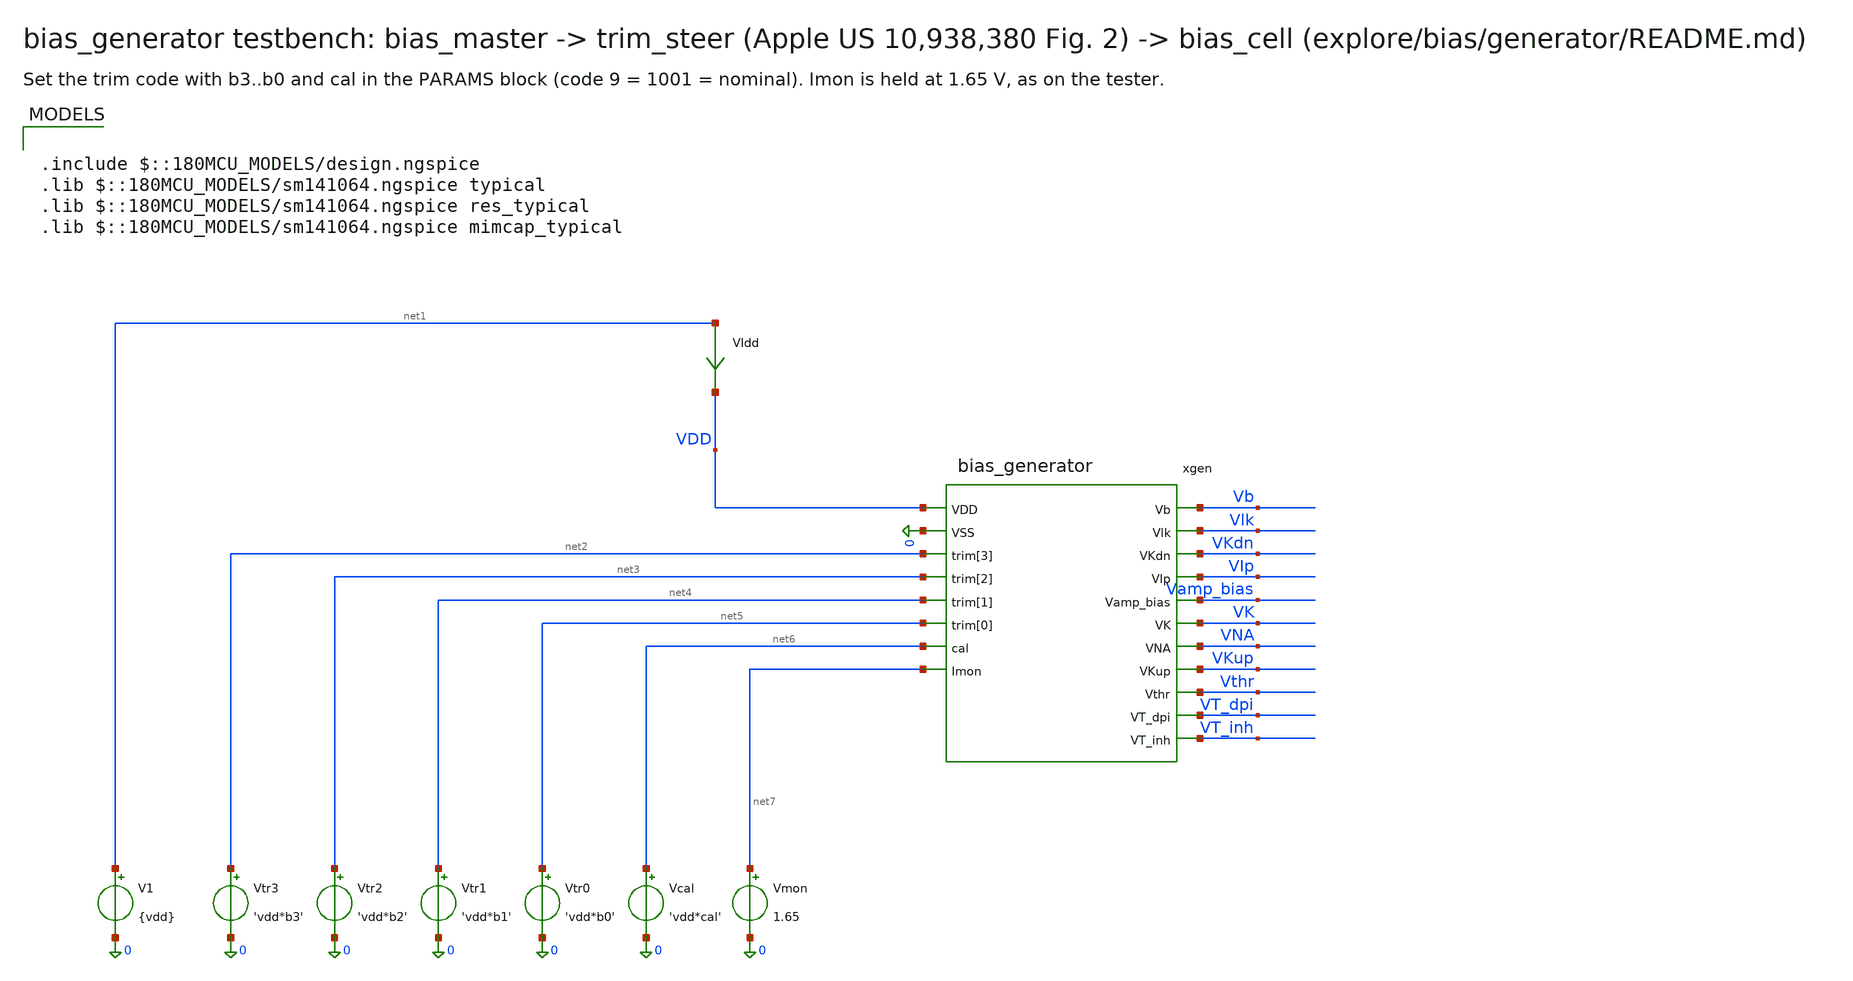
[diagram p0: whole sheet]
** sch_path: explore/bias/generator/bias_generator_tb.sch
**.subckt bias_generator_tb
xgen VDD 0 net2 net3 net4 net5 net6 net7 Vb Vlk VKdn VIp Vamp_bias VK VNA VKup Vthr VT_dpi VT_inh
+ bias_generator
V1 net1 0 {vdd}
VIdd net1 VDD 0
.save i(vidd)
Vtr3 net2 0 'vdd*b3'
Vtr2 net3 0 'vdd*b2'
Vtr1 net4 0 'vdd*b1'
Vtr0 net5 0 'vdd*b0'
Vcal net6 0 'vdd*cal'
Vmon net7 0 1.65
.save i(vmon)
**** begin user architecture code

.include $::180MCU_MODELS/design.ngspice
.lib $::180MCU_MODELS/sm141064.ngspice typical
.lib $::180MCU_MODELS/sm141064.ngspice res_typical
.lib $::180MCU_MODELS/sm141064.ngspice mimcap_typical



* trim code 9 = 1001 (nominal); ss chips trim to about 14, ff to about 4
* cal = 1 while trimming (aux path on: glitch-free code changes), 0 afterwards
.param vdd=3.3 b3=1 b2=0 b1=0 b0=1 cal=0
.temp 27




.control
save all
op
let imon_nA = -i(Vmon)*1e9
let supply_uA = i(VIdd)*1e6
print imon_nA supply_uA
print v(Vb) v(Vlk) v(VKdn) v(VIp) v(Vamp_bias) v(VK) v(VNA) v(VKup) v(Vthr) v(VT_dpi) v(VT_inh)
dc V1 2.97 3.63 0.03
plot v(Vb) v(Vlk) v(VKdn) v(VIp)
.endc


**** end user architecture code
**.ends

* expanding   symbol:  explore/bias/generator/bias_generator.sym # of pins=19
** sym_path: analog/bias/generator/bias_generator.sym
** sch_path: analog/bias/generator/bias_generator.sch
.subckt bias_generator VDD VSS trim[3] trim[2] trim[1] trim[0] cal Imon Vb Vlk VKdn VIp Vamp_bias VK
+ VNA VKup Vthr VT_dpi VT_inh
*.iopin VDD
*.iopin VSS
*.ipin trim[3]
*.ipin trim[2]
*.ipin trim[1]
*.ipin trim[0]
*.ipin cal
*.iopin Imon
*.opin Vb
*.opin Vlk
*.opin VKdn
*.opin VIp
*.opin Vamp_bias
*.opin VK
*.opin VNA
*.opin VKup
*.opin Vthr
*.opin VT_dpi
*.opin VT_inh
xmaster VDD VSS Iref bias_master
xtrim VDD VSS Iref Ibias trim[3] trim[2] trim[1] trim[0] cal trim_steer
xcell VDD VSS Ibias Vb Vlk VKdn VIp Vamp_bias VK VNA VKup Vthr VT_dpi VT_inh bias_cell
XMMON Imon Ibias VSS VSS nfet_03v3 L=8.0u W=10.0u nf=1 ad='int((nf+1)/2) * W/nf * 0.18u' as='int((nf+2)/2) * W/nf * 0.18u'
+ pd='2*int((nf+1)/2) * (W/nf + 0.18u)' ps='2*int((nf+2)/2) * (W/nf + 0.18u)' nrd='0.18u / W' nrs='0.18u / W'
+ sa=0 sb=0 sd=0 m=1
.ends


* expanding   symbol:  analog/bias/generator/bias_master.sym # of pins=3
** sym_path: analog/bias/generator/bias_master.sym
** sch_path: analog/bias/generator/bias_master.sch
.subckt bias_master VDD VSS Iref
*.iopin VDD
*.iopin VSS
*.iopin Iref
XM3 Vgp Vgp VDD VDD pfet_03v3 L=6.0u W=1.0u nf=1 ad='int((nf+1)/2) * W/nf * 0.18u' as='int((nf+2)/2) * W/nf * 0.18u'
+ pd='2*int((nf+1)/2) * (W/nf + 0.18u)' ps='2*int((nf+2)/2) * (W/nf + 0.18u)' nrd='0.18u / W' nrs='0.18u / W'
+ sa=0 sb=0 sd=0 m=4
XM4 Vgn Vgp VDD VDD pfet_03v3 L=6.0u W=1.0u nf=1 ad='int((nf+1)/2) * W/nf * 0.18u' as='int((nf+2)/2) * W/nf * 0.18u'
+ pd='2*int((nf+1)/2) * (W/nf + 0.18u)' ps='2*int((nf+2)/2) * (W/nf + 0.18u)' nrd='0.18u / W' nrs='0.18u / W'
+ sa=0 sb=0 sd=0 m=4
XM2 Vgp Vgn Vr VSS nfet_03v3 L=6.0u W=1.0u nf=1 ad='int((nf+1)/2) * W/nf * 0.18u' as='int((nf+2)/2) * W/nf * 0.18u'
+ pd='2*int((nf+1)/2) * (W/nf + 0.18u)' ps='2*int((nf+2)/2) * (W/nf + 0.18u)' nrd='0.18u / W' nrs='0.18u / W'
+ sa=0 sb=0 sd=0 m=64
XM1 Vgn Vgn VSS VSS nfet_03v3 L=6.0u W=1.0u nf=1 ad='int((nf+1)/2) * W/nf * 0.18u' as='int((nf+2)/2) * W/nf * 0.18u'
+ pd='2*int((nf+1)/2) * (W/nf + 0.18u)' ps='2*int((nf+2)/2) * (W/nf + 0.18u)' nrd='0.18u / W' nrs='0.18u / W'
+ sa=0 sb=0 sd=0 m=8
XR VSS Vr VSS nwell r_width=2.0e-6 r_length=585.380e-6 m=1
XMS1_0 net1 VSS VDD VDD pfet_03v3 L=45.45u W=0.5u nf=1 ad='int((nf+1)/2) * W/nf * 0.18u' as='int((nf+2)/2) * W/nf * 0.18u'
+ pd='2*int((nf+1)/2) * (W/nf + 0.18u)' ps='2*int((nf+2)/2) * (W/nf + 0.18u)' nrd='0.18u / W' nrs='0.18u / W'
+ sa=0 sb=0 sd=0 m=1
XMS1_1 net2 VSS net1 VDD pfet_03v3 L=45.45u W=0.5u nf=1 ad='int((nf+1)/2) * W/nf * 0.18u' as='int((nf+2)/2) * W/nf * 0.18u'
+ pd='2*int((nf+1)/2) * (W/nf + 0.18u)' ps='2*int((nf+2)/2) * (W/nf + 0.18u)' nrd='0.18u / W' nrs='0.18u / W'
+ sa=0 sb=0 sd=0 m=1
XMS1_2 net3 VSS net2 VDD pfet_03v3 L=45.45u W=0.5u nf=1 ad='int((nf+1)/2) * W/nf * 0.18u' as='int((nf+2)/2) * W/nf * 0.18u'
+ pd='2*int((nf+1)/2) * (W/nf + 0.18u)' ps='2*int((nf+2)/2) * (W/nf + 0.18u)' nrd='0.18u / W' nrs='0.18u / W'
+ sa=0 sb=0 sd=0 m=1
XMS1_3 s4 VSS net3 VDD pfet_03v3 L=45.45u W=0.5u nf=1 ad='int((nf+1)/2) * W/nf * 0.18u' as='int((nf+2)/2) * W/nf * 0.18u'
+ pd='2*int((nf+1)/2) * (W/nf + 0.18u)' ps='2*int((nf+2)/2) * (W/nf + 0.18u)' nrd='0.18u / W' nrs='0.18u / W'
+ sa=0 sb=0 sd=0 m=1
XMS2 X Vgn VSS VSS nfet_03v3 L=6.0u W=1.0u nf=1 ad='int((nf+1)/2) * W/nf * 0.18u' as='int((nf+2)/2) * W/nf * 0.18u'
+ pd='2*int((nf+1)/2) * (W/nf + 0.18u)' ps='2*int((nf+2)/2) * (W/nf + 0.18u)' nrd='0.18u / W' nrs='0.18u / W'
+ sa=0 sb=0 sd=0 m=16
XMS3 Vgp X VSS VSS nfet_03v3 L=4u W=0.5u nf=1 ad='int((nf+1)/2) * W/nf * 0.18u' as='int((nf+2)/2) * W/nf * 0.18u'
+ pd='2*int((nf+1)/2) * (W/nf + 0.18u)' ps='2*int((nf+2)/2) * (W/nf + 0.18u)' nrd='0.18u / W' nrs='0.18u / W'
+ sa=0 sb=0 sd=0 m=1
XMREF Iref Vgn VSS VSS nfet_03v3 L=6.0u W=1.0u nf=1 ad='int((nf+1)/2) * W/nf * 0.18u' as='int((nf+2)/2) * W/nf * 0.18u'
+ pd='2*int((nf+1)/2) * (W/nf + 0.18u)' ps='2*int((nf+2)/2) * (W/nf + 0.18u)' nrd='0.18u / W' nrs='0.18u / W'
+ sa=0 sb=0 sd=0 m=4
XMS1_4 net4 VSS s4 VDD pfet_03v3 L=45.45u W=0.5u nf=1 ad='int((nf+1)/2) * W/nf * 0.18u' as='int((nf+2)/2) * W/nf * 0.18u'
+ pd='2*int((nf+1)/2) * (W/nf + 0.18u)' ps='2*int((nf+2)/2) * (W/nf + 0.18u)' nrd='0.18u / W' nrs='0.18u / W'
+ sa=0 sb=0 sd=0 m=1
XMS1_5 net5 VSS net4 VDD pfet_03v3 L=45.45u W=0.5u nf=1 ad='int((nf+1)/2) * W/nf * 0.18u' as='int((nf+2)/2) * W/nf * 0.18u'
+ pd='2*int((nf+1)/2) * (W/nf + 0.18u)' ps='2*int((nf+2)/2) * (W/nf + 0.18u)' nrd='0.18u / W' nrs='0.18u / W'
+ sa=0 sb=0 sd=0 m=1
XMS1_6 net6 VSS net5 VDD pfet_03v3 L=45.45u W=0.5u nf=1 ad='int((nf+1)/2) * W/nf * 0.18u' as='int((nf+2)/2) * W/nf * 0.18u'
+ pd='2*int((nf+1)/2) * (W/nf + 0.18u)' ps='2*int((nf+2)/2) * (W/nf + 0.18u)' nrd='0.18u / W' nrs='0.18u / W'
+ sa=0 sb=0 sd=0 m=1
XMS1_7 net7 VSS net6 VDD pfet_03v3 L=45.45u W=0.5u nf=1 ad='int((nf+1)/2) * W/nf * 0.18u' as='int((nf+2)/2) * W/nf * 0.18u'
+ pd='2*int((nf+1)/2) * (W/nf + 0.18u)' ps='2*int((nf+2)/2) * (W/nf + 0.18u)' nrd='0.18u / W' nrs='0.18u / W'
+ sa=0 sb=0 sd=0 m=1
XMS1_8 net8 VSS net7 VDD pfet_03v3 L=45.45u W=0.5u nf=1 ad='int((nf+1)/2) * W/nf * 0.18u' as='int((nf+2)/2) * W/nf * 0.18u'
+ pd='2*int((nf+1)/2) * (W/nf + 0.18u)' ps='2*int((nf+2)/2) * (W/nf + 0.18u)' nrd='0.18u / W' nrs='0.18u / W'
+ sa=0 sb=0 sd=0 m=1
XMS1_9 X VSS net8 VDD pfet_03v3 L=45.45u W=0.5u nf=1 ad='int((nf+1)/2) * W/nf * 0.18u' as='int((nf+2)/2) * W/nf * 0.18u'
+ pd='2*int((nf+1)/2) * (W/nf + 0.18u)' ps='2*int((nf+2)/2) * (W/nf + 0.18u)' nrd='0.18u / W' nrs='0.18u / W'
+ sa=0 sb=0 sd=0 m=1
.ends


* expanding   symbol:  analog/bias/generator/trim_steer.sym # of pins=9
** sym_path: analog/bias/generator/trim_steer.sym
** sch_path: analog/bias/generator/trim_steer.sch
.subckt trim_steer VDD VSS Iref Ibias trim[3] trim[2] trim[1] trim[0] cal
*.iopin VDD
*.iopin VSS
*.iopin Iref
*.ipin trim[3]
*.ipin trim[2]
*.ipin trim[1]
*.ipin trim[0]
*.ipin cal
*.opin Ibias
XM0 Iref Iref VDD VDD pfet_03v3 L=6.0u W=1.0u nf=1 ad='int((nf+1)/2) * W/nf * 0.18u' as='int((nf+2)/2) * W/nf * 0.18u'
+ pd='2*int((nf+1)/2) * (W/nf + 0.18u)' ps='2*int((nf+2)/2) * (W/nf + 0.18u)' nrd='0.18u / W' nrs='0.18u / W'
+ sa=0 sb=0 sd=0 m=23
XR0 Iref Vgs VSS nwell r_width=2.0e-6 r_length=150.000e-6 m=1
XMCG VDD Vgs VDD VDD pfet_03v3 L=10.0u W=10.0u nf=1 ad='int((nf+1)/2) * W/nf * 0.18u' as='int((nf+2)/2) * W/nf * 0.18u'
+ pd='2*int((nf+1)/2) * (W/nf + 0.18u)' ps='2*int((nf+2)/2) * (W/nf + 0.18u)' nrd='0.18u / W' nrs='0.18u / W'
+ sa=0 sb=0 sd=0 m=1
XMB net1 Vgs VDD VDD pfet_03v3 L=6.0u W=1.0u nf=1 ad='int((nf+1)/2) * W/nf * 0.18u' as='int((nf+2)/2) * W/nf * 0.18u'
+ pd='2*int((nf+1)/2) * (W/nf + 0.18u)' ps='2*int((nf+2)/2) * (W/nf + 0.18u)' nrd='0.18u / W' nrs='0.18u / W'
+ sa=0 sb=0 sd=0 m=14
XSB net1 VDD Ibias VSS nfet_03v3 L=0.5u W=1.0u nf=1 ad='int((nf+1)/2) * W/nf * 0.18u' as='int((nf+2)/2) * W/nf * 0.18u'
+ pd='2*int((nf+1)/2) * (W/nf + 0.18u)' ps='2*int((nf+2)/2) * (W/nf + 0.18u)' nrd='0.18u / W' nrs='0.18u / W'
+ sa=0 sb=0 sd=0 m=1
XM1 net2 Vgs VDD VDD pfet_03v3 L=6.0u W=1.0u nf=1 ad='int((nf+1)/2) * W/nf * 0.18u' as='int((nf+2)/2) * W/nf * 0.18u'
+ pd='2*int((nf+1)/2) * (W/nf + 0.18u)' ps='2*int((nf+2)/2) * (W/nf + 0.18u)' nrd='0.18u / W' nrs='0.18u / W'
+ sa=0 sb=0 sd=0 m=1
XS0 net2 trim[0] Ibias VSS nfet_03v3 L=0.5u W=1.0u nf=1 ad='int((nf+1)/2) * W/nf * 0.18u' as='int((nf+2)/2) * W/nf * 0.18u'
+ pd='2*int((nf+1)/2) * (W/nf + 0.18u)' ps='2*int((nf+2)/2) * (W/nf + 0.18u)' nrd='0.18u / W' nrs='0.18u / W'
+ sa=0 sb=0 sd=0 m=1
XS0X net2 tb0 aux VSS nfet_03v3 L=0.5u W=1.0u nf=1 ad='int((nf+1)/2) * W/nf * 0.18u' as='int((nf+2)/2) * W/nf * 0.18u'
+ pd='2*int((nf+1)/2) * (W/nf + 0.18u)' ps='2*int((nf+2)/2) * (W/nf + 0.18u)' nrd='0.18u / W' nrs='0.18u / W'
+ sa=0 sb=0 sd=0 m=1
XM2 net3 Vgs VDD VDD pfet_03v3 L=6.0u W=1.0u nf=1 ad='int((nf+1)/2) * W/nf * 0.18u' as='int((nf+2)/2) * W/nf * 0.18u'
+ pd='2*int((nf+1)/2) * (W/nf + 0.18u)' ps='2*int((nf+2)/2) * (W/nf + 0.18u)' nrd='0.18u / W' nrs='0.18u / W'
+ sa=0 sb=0 sd=0 m=2
XS1 net3 trim[1] Ibias VSS nfet_03v3 L=0.5u W=1.0u nf=1 ad='int((nf+1)/2) * W/nf * 0.18u' as='int((nf+2)/2) * W/nf * 0.18u'
+ pd='2*int((nf+1)/2) * (W/nf + 0.18u)' ps='2*int((nf+2)/2) * (W/nf + 0.18u)' nrd='0.18u / W' nrs='0.18u / W'
+ sa=0 sb=0 sd=0 m=1
XS1X net3 tb1 aux VSS nfet_03v3 L=0.5u W=1.0u nf=1 ad='int((nf+1)/2) * W/nf * 0.18u' as='int((nf+2)/2) * W/nf * 0.18u'
+ pd='2*int((nf+1)/2) * (W/nf + 0.18u)' ps='2*int((nf+2)/2) * (W/nf + 0.18u)' nrd='0.18u / W' nrs='0.18u / W'
+ sa=0 sb=0 sd=0 m=1
XM3 net4 Vgs VDD VDD pfet_03v3 L=6.0u W=1.0u nf=1 ad='int((nf+1)/2) * W/nf * 0.18u' as='int((nf+2)/2) * W/nf * 0.18u'
+ pd='2*int((nf+1)/2) * (W/nf + 0.18u)' ps='2*int((nf+2)/2) * (W/nf + 0.18u)' nrd='0.18u / W' nrs='0.18u / W'
+ sa=0 sb=0 sd=0 m=4
XS2 net4 trim[2] Ibias VSS nfet_03v3 L=0.5u W=1.0u nf=1 ad='int((nf+1)/2) * W/nf * 0.18u' as='int((nf+2)/2) * W/nf * 0.18u'
+ pd='2*int((nf+1)/2) * (W/nf + 0.18u)' ps='2*int((nf+2)/2) * (W/nf + 0.18u)' nrd='0.18u / W' nrs='0.18u / W'
+ sa=0 sb=0 sd=0 m=1
XS2X net4 tb2 aux VSS nfet_03v3 L=0.5u W=1.0u nf=1 ad='int((nf+1)/2) * W/nf * 0.18u' as='int((nf+2)/2) * W/nf * 0.18u'
+ pd='2*int((nf+1)/2) * (W/nf + 0.18u)' ps='2*int((nf+2)/2) * (W/nf + 0.18u)' nrd='0.18u / W' nrs='0.18u / W'
+ sa=0 sb=0 sd=0 m=1
XM4 net5 Vgs VDD VDD pfet_03v3 L=6.0u W=1.0u nf=1 ad='int((nf+1)/2) * W/nf * 0.18u' as='int((nf+2)/2) * W/nf * 0.18u'
+ pd='2*int((nf+1)/2) * (W/nf + 0.18u)' ps='2*int((nf+2)/2) * (W/nf + 0.18u)' nrd='0.18u / W' nrs='0.18u / W'
+ sa=0 sb=0 sd=0 m=8
XS3 net5 trim[3] Ibias VSS nfet_03v3 L=0.5u W=1.0u nf=1 ad='int((nf+1)/2) * W/nf * 0.18u' as='int((nf+2)/2) * W/nf * 0.18u'
+ pd='2*int((nf+1)/2) * (W/nf + 0.18u)' ps='2*int((nf+2)/2) * (W/nf + 0.18u)' nrd='0.18u / W' nrs='0.18u / W'
+ sa=0 sb=0 sd=0 m=1
XS3X net5 tb3 aux VSS nfet_03v3 L=0.5u W=1.0u nf=1 ad='int((nf+1)/2) * W/nf * 0.18u' as='int((nf+2)/2) * W/nf * 0.18u'
+ pd='2*int((nf+1)/2) * (W/nf + 0.18u)' ps='2*int((nf+2)/2) * (W/nf + 0.18u)' nrd='0.18u / W' nrs='0.18u / W'
+ sa=0 sb=0 sd=0 m=1
XMIP0 tb0 trim[0] VDD VDD pfet_03v3 L=0.28u W=1.0u nf=1 ad='int((nf+1)/2) * W/nf * 0.18u' as='int((nf+2)/2) * W/nf * 0.18u'
+ pd='2*int((nf+1)/2) * (W/nf + 0.18u)' ps='2*int((nf+2)/2) * (W/nf + 0.18u)' nrd='0.18u / W' nrs='0.18u / W'
+ sa=0 sb=0 sd=0 m=1
XMIN0 tb0 trim[0] VSS VSS nfet_03v3 L=0.28u W=0.5u nf=1 ad='int((nf+1)/2) * W/nf * 0.18u' as='int((nf+2)/2) * W/nf * 0.18u'
+ pd='2*int((nf+1)/2) * (W/nf + 0.18u)' ps='2*int((nf+2)/2) * (W/nf + 0.18u)' nrd='0.18u / W' nrs='0.18u / W'
+ sa=0 sb=0 sd=0 m=1
XMIP1 tb1 trim[1] VDD VDD pfet_03v3 L=0.28u W=1.0u nf=1 ad='int((nf+1)/2) * W/nf * 0.18u' as='int((nf+2)/2) * W/nf * 0.18u'
+ pd='2*int((nf+1)/2) * (W/nf + 0.18u)' ps='2*int((nf+2)/2) * (W/nf + 0.18u)' nrd='0.18u / W' nrs='0.18u / W'
+ sa=0 sb=0 sd=0 m=1
XMIN1 tb1 trim[1] VSS VSS nfet_03v3 L=0.28u W=0.5u nf=1 ad='int((nf+1)/2) * W/nf * 0.18u' as='int((nf+2)/2) * W/nf * 0.18u'
+ pd='2*int((nf+1)/2) * (W/nf + 0.18u)' ps='2*int((nf+2)/2) * (W/nf + 0.18u)' nrd='0.18u / W' nrs='0.18u / W'
+ sa=0 sb=0 sd=0 m=1
XMIP2 tb2 trim[2] VDD VDD pfet_03v3 L=0.28u W=1.0u nf=1 ad='int((nf+1)/2) * W/nf * 0.18u' as='int((nf+2)/2) * W/nf * 0.18u'
+ pd='2*int((nf+1)/2) * (W/nf + 0.18u)' ps='2*int((nf+2)/2) * (W/nf + 0.18u)' nrd='0.18u / W' nrs='0.18u / W'
+ sa=0 sb=0 sd=0 m=1
XMIN2 tb2 trim[2] VSS VSS nfet_03v3 L=0.28u W=0.5u nf=1 ad='int((nf+1)/2) * W/nf * 0.18u' as='int((nf+2)/2) * W/nf * 0.18u'
+ pd='2*int((nf+1)/2) * (W/nf + 0.18u)' ps='2*int((nf+2)/2) * (W/nf + 0.18u)' nrd='0.18u / W' nrs='0.18u / W'
+ sa=0 sb=0 sd=0 m=1
XMIP3 tb3 trim[3] VDD VDD pfet_03v3 L=0.28u W=1.0u nf=1 ad='int((nf+1)/2) * W/nf * 0.18u' as='int((nf+2)/2) * W/nf * 0.18u'
+ pd='2*int((nf+1)/2) * (W/nf + 0.18u)' ps='2*int((nf+2)/2) * (W/nf + 0.18u)' nrd='0.18u / W' nrs='0.18u / W'
+ sa=0 sb=0 sd=0 m=1
XMIN3 tb3 trim[3] VSS VSS nfet_03v3 L=0.28u W=0.5u nf=1 ad='int((nf+1)/2) * W/nf * 0.18u' as='int((nf+2)/2) * W/nf * 0.18u'
+ pd='2*int((nf+1)/2) * (W/nf + 0.18u)' ps='2*int((nf+2)/2) * (W/nf + 0.18u)' nrd='0.18u / W' nrs='0.18u / W'
+ sa=0 sb=0 sd=0 m=1
XMAUX aux vaux VSS VSS nfet_03v3 L=8.0u W=10.0u nf=1 ad='int((nf+1)/2) * W/nf * 0.18u' as='int((nf+2)/2) * W/nf * 0.18u'
+ pd='2*int((nf+1)/2) * (W/nf + 0.18u)' ps='2*int((nf+2)/2) * (W/nf + 0.18u)' nrd='0.18u / W' nrs='0.18u / W'
+ sa=0 sb=0 sd=0 m=1
XMCAL aux cal vaux VSS nfet_03v3 L=0.5u W=1.0u nf=1 ad='int((nf+1)/2) * W/nf * 0.18u' as='int((nf+2)/2) * W/nf * 0.18u'
+ pd='2*int((nf+1)/2) * (W/nf + 0.18u)' ps='2*int((nf+2)/2) * (W/nf + 0.18u)' nrd='0.18u / W' nrs='0.18u / W'
+ sa=0 sb=0 sd=0 m=1
XMDIS vaux calb VSS VSS nfet_03v3 L=45.45u W=0.5u nf=1 ad='int((nf+1)/2) * W/nf * 0.18u' as='int((nf+2)/2) * W/nf * 0.18u'
+ pd='2*int((nf+1)/2) * (W/nf + 0.18u)' ps='2*int((nf+2)/2) * (W/nf + 0.18u)' nrd='0.18u / W' nrs='0.18u / W'
+ sa=0 sb=0 sd=0 m=1
XMCAUX VSS vaux VSS VSS nfet_03v3 L=5.0u W=5.0u nf=1 ad='int((nf+1)/2) * W/nf * 0.18u' as='int((nf+2)/2) * W/nf * 0.18u'
+ pd='2*int((nf+1)/2) * (W/nf + 0.18u)' ps='2*int((nf+2)/2) * (W/nf + 0.18u)' nrd='0.18u / W' nrs='0.18u / W'
+ sa=0 sb=0 sd=0 m=1
XMIPC calb cal VDD VDD pfet_03v3 L=0.28u W=1.0u nf=1 ad='int((nf+1)/2) * W/nf * 0.18u' as='int((nf+2)/2) * W/nf * 0.18u'
+ pd='2*int((nf+1)/2) * (W/nf + 0.18u)' ps='2*int((nf+2)/2) * (W/nf + 0.18u)' nrd='0.18u / W' nrs='0.18u / W'
+ sa=0 sb=0 sd=0 m=1
XMINC calb cal VSS VSS nfet_03v3 L=0.28u W=0.5u nf=1 ad='int((nf+1)/2) * W/nf * 0.18u' as='int((nf+2)/2) * W/nf * 0.18u'
+ pd='2*int((nf+1)/2) * (W/nf + 0.18u)' ps='2*int((nf+2)/2) * (W/nf + 0.18u)' nrd='0.18u / W' nrs='0.18u / W'
+ sa=0 sb=0 sd=0 m=1
.ends


* expanding   symbol:  bias_cell.sym # of pins=14
** sym_path: analog/neuron/bias_cell.sym
** sch_path: analog/neuron/bias_cell.sch
.subckt bias_cell VDD VSS Iref Vb Vlk VKdn VIp Vamp_bias VK VNA VKup Vthr VT_dpi VT_inh
*.iopin VDD
*.iopin VSS
*.iopin Iref
*.opin Vb
*.opin Vlk
*.opin VKdn
*.opin VIp
*.opin Vamp_bias
*.opin VK
*.opin VNA
*.opin VKup
*.opin Vthr
*.opin VT_dpi
*.opin VT_inh
XMN0 Iref Iref VSS VSS nfet_03v3 L=8u W=10u nf=1 ad='int((nf+1)/2) * W/nf * 0.18u' as='int((nf+2)/2) * W/nf * 0.18u'
+ pd='2*int((nf+1)/2) * (W/nf + 0.18u)' ps='2*int((nf+2)/2) * (W/nf + 0.18u)' nrd='0.18u / W' nrs='0.18u / W'
+ sa=0 sb=0 sd=0 m=1
XMNP vgp Iref VSS VSS nfet_03v3 L=8u W=10u nf=1 ad='int((nf+1)/2) * W/nf * 0.18u' as='int((nf+2)/2) * W/nf * 0.18u'
+ pd='2*int((nf+1)/2) * (W/nf + 0.18u)' ps='2*int((nf+2)/2) * (W/nf + 0.18u)' nrd='0.18u / W' nrs='0.18u / W'
+ sa=0 sb=0 sd=0 m=1
XMP0 vgp vgp VDD VDD pfet_03v3 L=8u W=10u nf=1 ad='int((nf+1)/2) * W/nf * 0.18u' as='int((nf+2)/2) * W/nf * 0.18u'
+ pd='2*int((nf+1)/2) * (W/nf + 0.18u)' ps='2*int((nf+2)/2) * (W/nf + 0.18u)' nrd='0.18u / W' nrs='0.18u / W'
+ sa=0 sb=0 sd=0 m=1
XMO_Vb Vb vgp VDD VDD pfet_03v3 L=8u W=1.435u nf=1 ad='int((nf+1)/2) * W/nf * 0.18u' as='int((nf+2)/2) * W/nf * 0.18u'
+ pd='2*int((nf+1)/2) * (W/nf + 0.18u)' ps='2*int((nf+2)/2) * (W/nf + 0.18u)' nrd='0.18u / W' nrs='0.18u / W'
+ sa=0 sb=0 sd=0 m=1
XMR_Vb Vb Vb VSS VSS nfet_03v3 L=8u W=1u nf=1 ad='int((nf+1)/2) * W/nf * 0.18u' as='int((nf+2)/2) * W/nf * 0.18u'
+ pd='2*int((nf+1)/2) * (W/nf + 0.18u)' ps='2*int((nf+2)/2) * (W/nf + 0.18u)' nrd='0.18u / W' nrs='0.18u / W'
+ sa=0 sb=0 sd=0 m=1
XMO_Vlk Vlk vgp VDD VDD pfet_03v3 L=16u W=0.84u nf=1 ad='int((nf+1)/2) * W/nf * 0.18u' as='int((nf+2)/2) * W/nf * 0.18u'
+ pd='2*int((nf+1)/2) * (W/nf + 0.18u)' ps='2*int((nf+2)/2) * (W/nf + 0.18u)' nrd='0.18u / W' nrs='0.18u / W'
+ sa=0 sb=0 sd=0 m=1
XMR_Vlk Vlk Vlk VSS VSS nfet_03v3 L=1u W=1u nf=1 ad='int((nf+1)/2) * W/nf * 0.18u' as='int((nf+2)/2) * W/nf * 0.18u'
+ pd='2*int((nf+1)/2) * (W/nf + 0.18u)' ps='2*int((nf+2)/2) * (W/nf + 0.18u)' nrd='0.18u / W' nrs='0.18u / W'
+ sa=0 sb=0 sd=0 m=8
XMO_VKdn VKdn vgp VDD VDD pfet_03v3 L=8u W=12.94u nf=1 ad='int((nf+1)/2) * W/nf * 0.18u' as='int((nf+2)/2) * W/nf * 0.18u'
+ pd='2*int((nf+1)/2) * (W/nf + 0.18u)' ps='2*int((nf+2)/2) * (W/nf + 0.18u)' nrd='0.18u / W' nrs='0.18u / W'
+ sa=0 sb=0 sd=0 m=1
XMR_VKdn VKdn VKdn VSS VSS nfet_03v3 L=1u W=1u nf=1 ad='int((nf+1)/2) * W/nf * 0.18u' as='int((nf+2)/2) * W/nf * 0.18u'
+ pd='2*int((nf+1)/2) * (W/nf + 0.18u)' ps='2*int((nf+2)/2) * (W/nf + 0.18u)' nrd='0.18u / W' nrs='0.18u / W'
+ sa=0 sb=0 sd=0 m=4
XMO_VIp VIp vgp VDD VDD pfet_03v3 L=8u W=2.335u nf=1 ad='int((nf+1)/2) * W/nf * 0.18u' as='int((nf+2)/2) * W/nf * 0.18u'
+ pd='2*int((nf+1)/2) * (W/nf + 0.18u)' ps='2*int((nf+2)/2) * (W/nf + 0.18u)' nrd='0.18u / W' nrs='0.18u / W'
+ sa=0 sb=0 sd=0 m=1
XMR_VIp VIp VIp VSS VSS nfet_03v3 L=1u W=1u nf=1 ad='int((nf+1)/2) * W/nf * 0.18u' as='int((nf+2)/2) * W/nf * 0.18u'
+ pd='2*int((nf+1)/2) * (W/nf + 0.18u)' ps='2*int((nf+2)/2) * (W/nf + 0.18u)' nrd='0.18u / W' nrs='0.18u / W'
+ sa=0 sb=0 sd=0 m=1
XMO_Vamp_bias Vamp_bias vgp VDD VDD pfet_03v3 L=8u W=9.14u nf=1 ad='int((nf+1)/2) * W/nf * 0.18u' as='int((nf+2)/2) * W/nf * 0.18u'
+ pd='2*int((nf+1)/2) * (W/nf + 0.18u)' ps='2*int((nf+2)/2) * (W/nf + 0.18u)' nrd='0.18u / W' nrs='0.18u / W'
+ sa=0 sb=0 sd=0 m=1
XMR_Vamp_bias Vamp_bias Vamp_bias VSS VSS nfet_03v3 L=0.28u W=0.22u nf=1 ad='int((nf+1)/2) * W/nf * 0.18u'
+ as='int((nf+2)/2) * W/nf * 0.18u' pd='2*int((nf+1)/2) * (W/nf + 0.18u)' ps='2*int((nf+2)/2) * (W/nf + 0.18u)'
+ nrd='0.18u / W' nrs='0.18u / W' sa=0 sb=0 sd=0 m=1
XMO_VK VK vgp VDD VDD pfet_03v3 L=8u W=10.45u nf=1 ad='int((nf+1)/2) * W/nf * 0.18u' as='int((nf+2)/2) * W/nf * 0.18u'
+ pd='2*int((nf+1)/2) * (W/nf + 0.18u)' ps='2*int((nf+2)/2) * (W/nf + 0.18u)' nrd='0.18u / W' nrs='0.18u / W'
+ sa=0 sb=0 sd=0 m=1
XMR_VK VK VK VSS VSS nfet_03v3 L=40u W=0.22u nf=1 ad='int((nf+1)/2) * W/nf * 0.18u' as='int((nf+2)/2) * W/nf * 0.18u'
+ pd='2*int((nf+1)/2) * (W/nf + 0.18u)' ps='2*int((nf+2)/2) * (W/nf + 0.18u)' nrd='0.18u / W' nrs='0.18u / W'
+ sa=0 sb=0 sd=0 m=1
XMR_VNA VNA VNA VDD VDD pfet_03v3 L=20u W=0.22u nf=1 ad='int((nf+1)/2) * W/nf * 0.18u' as='int((nf+2)/2) * W/nf * 0.18u'
+ pd='2*int((nf+1)/2) * (W/nf + 0.18u)' ps='2*int((nf+2)/2) * (W/nf + 0.18u)' nrd='0.18u / W' nrs='0.18u / W'
+ sa=0 sb=0 sd=0 m=1
XMO_VNA VNA Iref VSS VSS nfet_03v3 L=8u W=5.755u nf=1 ad='int((nf+1)/2) * W/nf * 0.18u' as='int((nf+2)/2) * W/nf * 0.18u'
+ pd='2*int((nf+1)/2) * (W/nf + 0.18u)' ps='2*int((nf+2)/2) * (W/nf + 0.18u)' nrd='0.18u / W' nrs='0.18u / W'
+ sa=0 sb=0 sd=0 m=1
XMR_VKup VKup VKup VDD VDD pfet_03v3 L=8u W=1u nf=1 ad='int((nf+1)/2) * W/nf * 0.18u' as='int((nf+2)/2) * W/nf * 0.18u'
+ pd='2*int((nf+1)/2) * (W/nf + 0.18u)' ps='2*int((nf+2)/2) * (W/nf + 0.18u)' nrd='0.18u / W' nrs='0.18u / W'
+ sa=0 sb=0 sd=0 m=1
XMO_VKup VKup Iref VSS VSS nfet_03v3 L=8u W=6.005u nf=1 ad='int((nf+1)/2) * W/nf * 0.18u' as='int((nf+2)/2) * W/nf * 0.18u'
+ pd='2*int((nf+1)/2) * (W/nf + 0.18u)' ps='2*int((nf+2)/2) * (W/nf + 0.18u)' nrd='0.18u / W' nrs='0.18u / W'
+ sa=0 sb=0 sd=0 m=1
XMR_Vthr Vthr Vthr VDD VDD pfet_03v3 L=0.28u W=0.22u nf=1 ad='int((nf+1)/2) * W/nf * 0.18u' as='int((nf+2)/2) * W/nf * 0.18u'
+ pd='2*int((nf+1)/2) * (W/nf + 0.18u)' ps='2*int((nf+2)/2) * (W/nf + 0.18u)' nrd='0.18u / W' nrs='0.18u / W'
+ sa=0 sb=0 sd=0 m=32
XMO_Vthr Vthr Iref VSS VSS nfet_03v3 L=32u W=0.905u nf=1 ad='int((nf+1)/2) * W/nf * 0.18u' as='int((nf+2)/2) * W/nf * 0.18u'
+ pd='2*int((nf+1)/2) * (W/nf + 0.18u)' ps='2*int((nf+2)/2) * (W/nf + 0.18u)' nrd='0.18u / W' nrs='0.18u / W'
+ sa=0 sb=0 sd=0 m=1
XMR_VT_dpi VT_dpi VT_dpi VDD VDD pfet_03v3 L=0.28u W=0.22u nf=1 ad='int((nf+1)/2) * W/nf * 0.18u' as='int((nf+2)/2) * W/nf * 0.18u'
+ pd='2*int((nf+1)/2) * (W/nf + 0.18u)' ps='2*int((nf+2)/2) * (W/nf + 0.18u)' nrd='0.18u / W' nrs='0.18u / W'
+ sa=0 sb=0 sd=0 m=32
XMO_VT_dpi VT_dpi Iref VSS VSS nfet_03v3 L=32u W=1.165u nf=1 ad='int((nf+1)/2) * W/nf * 0.18u' as='int((nf+2)/2) * W/nf * 0.18u'
+ pd='2*int((nf+1)/2) * (W/nf + 0.18u)' ps='2*int((nf+2)/2) * (W/nf + 0.18u)' nrd='0.18u / W' nrs='0.18u / W'
+ sa=0 sb=0 sd=0 m=1
XMR_VT_inh VT_inh VT_inh VDD VDD pfet_03v3 L=1.12u W=0.88u nf=1 ad='int((nf+1)/2) * W/nf * 0.18u' as='int((nf+2)/2) * W/nf * 0.18u'
+ pd='2*int((nf+1)/2) * (W/nf + 0.18u)' ps='2*int((nf+2)/2) * (W/nf + 0.18u)' nrd='0.18u / W' nrs='0.18u / W'
+ sa=0 sb=0 sd=0 m=16
XMO_VT_inh VT_inh Iref VSS VSS nfet_03v3 L=32u W=0.625u nf=1 ad='int((nf+1)/2) * W/nf * 0.18u' as='int((nf+2)/2) * W/nf * 0.18u'
+ pd='2*int((nf+1)/2) * (W/nf + 0.18u)' ps='2*int((nf+2)/2) * (W/nf + 0.18u)' nrd='0.18u / W' nrs='0.18u / W'
+ sa=0 sb=0 sd=0 m=1
.ends

.end
